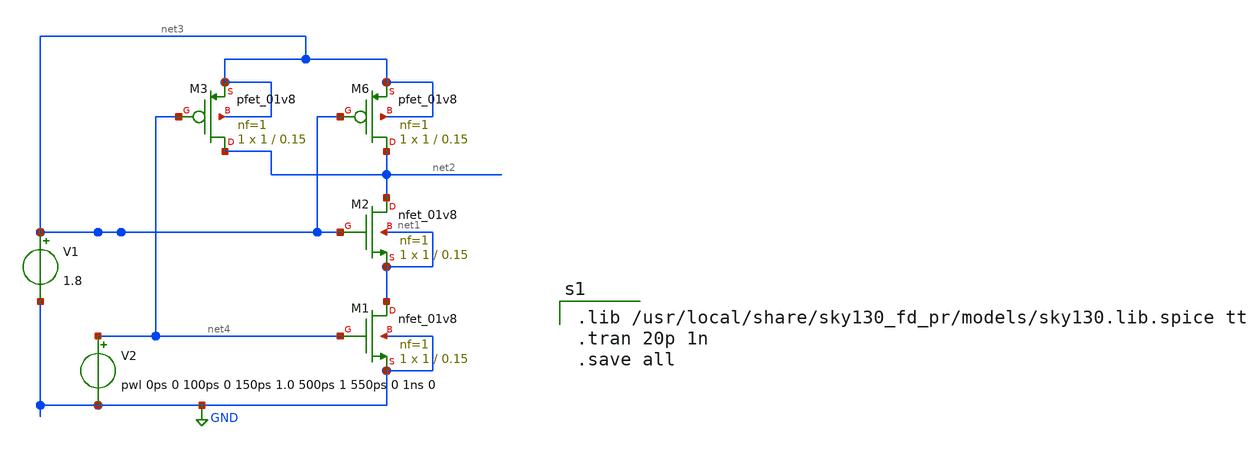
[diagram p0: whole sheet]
** sch_path: projects/nand/nand.sch
**.subckt nand
XM1 net1 net4 GND GND sky130_fd_pr__nfet_01v8 L=0.15 W=1 nf=1 ad='int((nf+1)/2) * W/nf * 0.29' as='int((nf+2)/2) * W/nf * 0.29'
+ pd='2*int((nf+1)/2) * (W/nf + 0.29)' ps='2*int((nf+2)/2) * (W/nf + 0.29)' nrd='0.29 / W' nrs='0.29 / W'
+ sa=0 sb=0 sd=0 mult=1 m=1
XM2 net2 net3 net1 net1 sky130_fd_pr__nfet_01v8 L=0.15 W=1 nf=1 ad='int((nf+1)/2) * W/nf * 0.29' as='int((nf+2)/2) * W/nf * 0.29'
+ pd='2*int((nf+1)/2) * (W/nf + 0.29)' ps='2*int((nf+2)/2) * (W/nf + 0.29)' nrd='0.29 / W' nrs='0.29 / W'
+ sa=0 sb=0 sd=0 mult=1 m=1
XM6 net2 net3 net3 net3 sky130_fd_pr__pfet_01v8 L=0.15 W=1 nf=1 ad='int((nf+1)/2) * W/nf * 0.29' as='int((nf+2)/2) * W/nf * 0.29'
+ pd='2*int((nf+1)/2) * (W/nf + 0.29)' ps='2*int((nf+2)/2) * (W/nf + 0.29)' nrd='0.29 / W' nrs='0.29 / W'
+ sa=0 sb=0 sd=0 mult=1 m=1
XM3 net2 net4 net3 net3 sky130_fd_pr__pfet_01v8 L=0.15 W=1 nf=1 ad='int((nf+1)/2) * W/nf * 0.29' as='int((nf+2)/2) * W/nf * 0.29'
+ pd='2*int((nf+1)/2) * (W/nf + 0.29)' ps='2*int((nf+2)/2) * (W/nf + 0.29)' nrd='0.29 / W' nrs='0.29 / W'
+ sa=0 sb=0 sd=0 mult=1 m=1
V1 net3 GND 1.8
V2 net4 GND pwl 0ps 0 100ps 0 150ps 1.0 500ps 1 550ps 0 1ns 0
**** begin user architecture code

.lib /usr/local/share/sky130_fd_pr/models/sky130.lib.spice tt
.tran 20p 1n
.save all

**** end user architecture code
**.ends
.GLOBAL GND
.end
